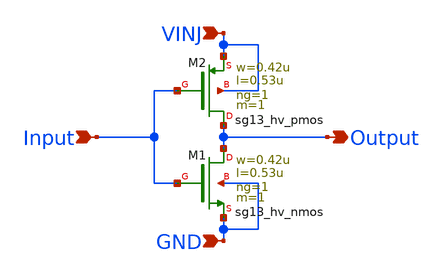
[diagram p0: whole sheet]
** sch_path: ihp130_cells/VinjInv2/ihp130_VinjInv2.sch
**.subckt ihp130_VinjInv2 VINJ GND Input Output
*.ipin VINJ
*.ipin GND
*.ipin Input
*.opin Output
XM1 Output Input GND GND sg13_hv_nmos w=0.42u l=0.53u ng=1 m=1 mm_ok=1
XM2 Output Input VINJ VINJ sg13_hv_pmos w=0.42u l=0.53u ng=1 m=1 mm_ok=1
**.ends
.end
